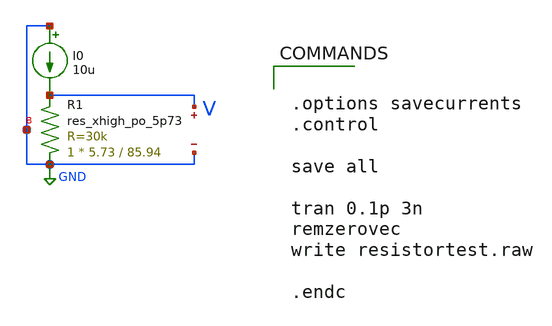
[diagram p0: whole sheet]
** sch_path: PTAT/xschem/resistortest.sch
.lib $::SKYWATER_MODELS/sky130.lib.spice tt
.include $::SKYWATER_STDCELLS/sky130_fd_sc_hd.spice

**.subckt resistortest
XR1 GND V GND sky130_fd_pr__res_xhigh_po_5p73 L=85.94 mult=1 m=1
I0 GND V 10u
.save v(v)
.save v(gnd)
**** begin user architecture code


.options savecurrents
.control

save all

tran 0.1p 3n
remzerovec
write resistortest.raw

.endc


**** end user architecture code
**.ends
.GLOBAL GND
.end
